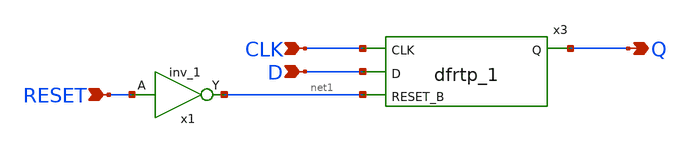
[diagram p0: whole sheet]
** sch_path: xschem/my_df.sch
**.subckt my_df CLK D RESET Q
*.ipin CLK
*.ipin D
*.ipin RESET
*.opin Q
x1 RESET GND GND VDD VDD net1 sky130_fd_sc_hd__inv_1
x3 CLK D net1 GND GND VDD VDD Q sky130_fd_sc_hd__dfrtp_1
**.ends
.end
